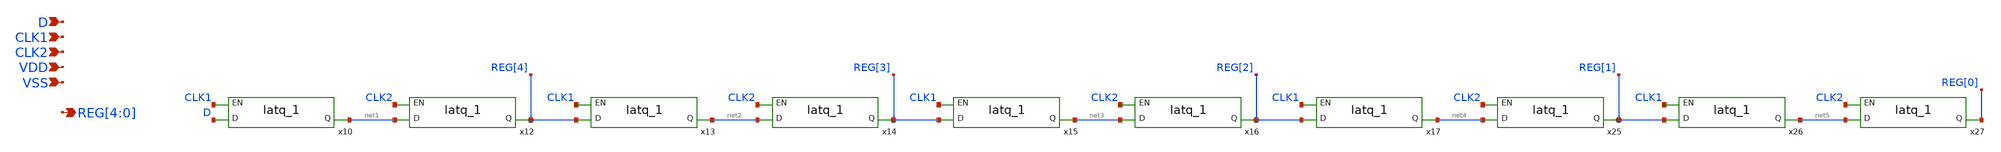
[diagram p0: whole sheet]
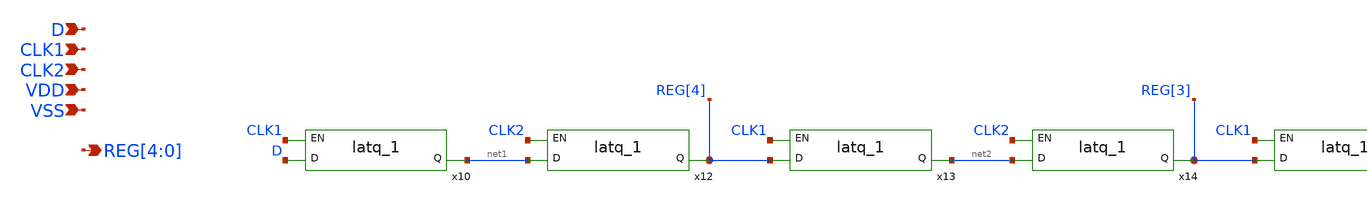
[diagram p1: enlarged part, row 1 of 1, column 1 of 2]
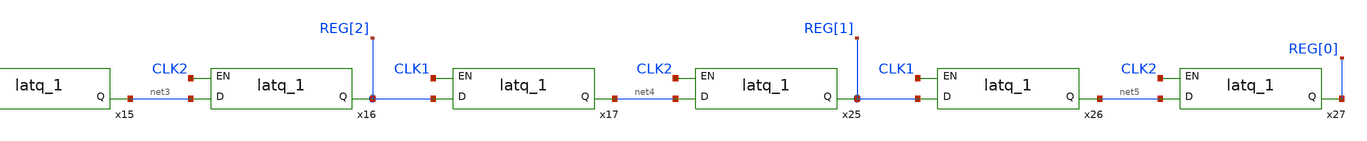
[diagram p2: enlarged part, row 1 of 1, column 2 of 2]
** sch_path: designs/libs/core_fpga/REG_BANK_5B/REG_BANK_5B.sch
**.subckt REG_BANK_5B D CLK1 CLK2 REG[4],REG[3],REG[2],REG[1],REG[0] VDD VSS
*.ipin D
*.ipin CLK1
*.ipin CLK2
*.opin REG[4],REG[3],REG[2],REG[1],REG[0]
*.ipin VDD
*.ipin VSS
x10 D CLK1 net1 VDD VDD VSS VSS gf180mcu_fd_sc_mcu9t5v0__latq_1
x12 net1 CLK2 REG[4] VDD VDD VSS VSS gf180mcu_fd_sc_mcu9t5v0__latq_1
x13 REG[4] CLK1 net2 VDD VDD VSS VSS gf180mcu_fd_sc_mcu9t5v0__latq_1
x14 net2 CLK2 REG[3] VDD VDD VSS VSS gf180mcu_fd_sc_mcu9t5v0__latq_1
x15 REG[3] CLK1 net3 VDD VDD VSS VSS gf180mcu_fd_sc_mcu9t5v0__latq_1
x16 net3 CLK2 REG[2] VDD VDD VSS VSS gf180mcu_fd_sc_mcu9t5v0__latq_1
x17 REG[2] CLK1 net4 VDD VDD VSS VSS gf180mcu_fd_sc_mcu9t5v0__latq_1
x25 net4 CLK2 REG[1] VDD VDD VSS VSS gf180mcu_fd_sc_mcu9t5v0__latq_1
x26 REG[1] CLK1 net5 VDD VDD VSS VSS gf180mcu_fd_sc_mcu9t5v0__latq_1
x27 net5 CLK2 REG[0] VDD VDD VSS VSS gf180mcu_fd_sc_mcu9t5v0__latq_1
**.ends
.end
